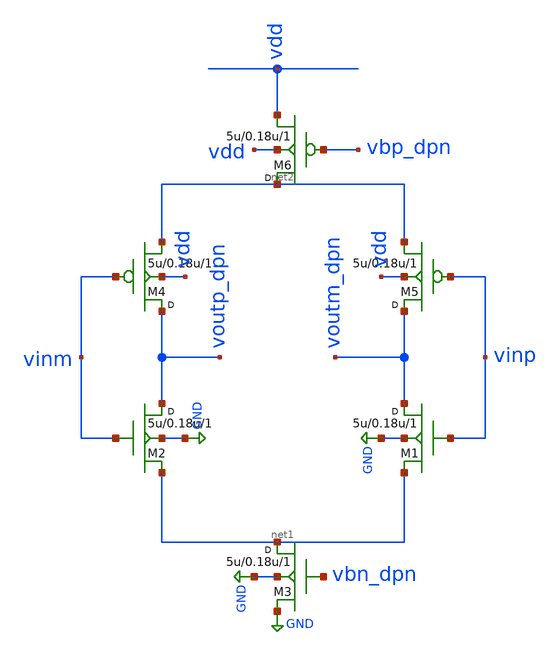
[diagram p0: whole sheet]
** sch_path: synthetic/blocks/diff_pair_nmos.sch
**.subckt diff_pair_nmos
M1 voutm_dpn vinp net1 GND nmos w=5u l=0.18u m=1
M2 voutp_dpn vinm net1 GND nmos w=5u l=0.18u m=1
M3 net1 vbn_dpn GND GND nmos w=5u l=0.18u m=1
M4 voutp_dpn vinm net2 vdd pmos w=5u l=0.18u m=1
M5 voutm_dpn vinp net2 vdd pmos w=5u l=0.18u m=1
M6 net2 vbp_dpn vdd vdd pmos w=5u l=0.18u m=1
**.ends
.GLOBAL GND
.end
